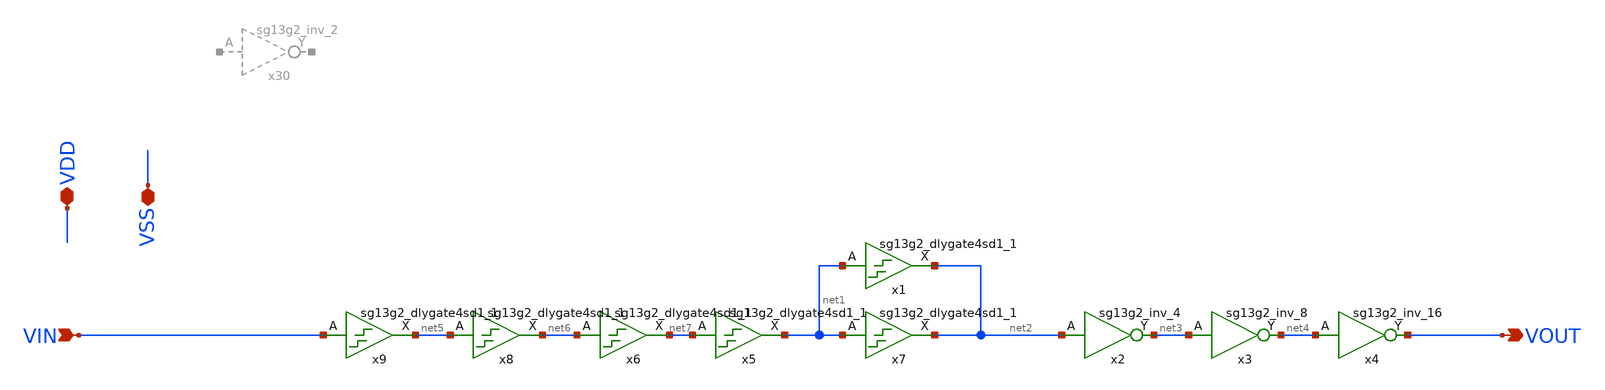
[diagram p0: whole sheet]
** sch_path: Cells/DLine.sch
* IHP-GmbH/IHP-Open-PDK/ihp-sg13g2/libs.tech/xschem/sg13g2_stdcells/sg13g2_inv_16.sch:
* Copyright 2023 IHP PDK Authors
* Licensed under the Apache License, Version 2.0 (the "License");
**.subckt DLine VOUT VIN VDD VSS
*.opin VOUT
*.ipin VIN
*.iopin VDD
*.iopin VSS
x7 net2 net1 VDD VSS sg13g2_dlygate4sd1_1
x1 net2 net1 VDD VSS sg13g2_dlygate4sd1_1
x2 net3 net2 VDD VSS sg13g2_inv_4
x3 net4 net3 VDD VSS sg13g2_inv_8
x4 VOUT net4 VDD VSS sg13g2_inv_16
x5 net1 net7 VDD VSS sg13g2_dlygate4sd1_1
x6 net7 net6 VDD VSS sg13g2_dlygate4sd1_1
x8 net6 net5 VDD VSS sg13g2_dlygate4sd1_1
x9 net5 VIN VDD VSS sg13g2_dlygate4sd1_1
**.ends

* expanding   symbol:  sg13g2_stdcells/sg13g2_dlygate4sd1_1.sym # of pins=2
** sym_path: sg13g2_stdcells/sg13g2_dlygate4sd1_1.sym
** sch_path: sg13g2_stdcells/sg13g2_dlygate4sd1_1.sch
.subckt sg13g2_dlygate4sd1_1 X A VDD VSS
*.ipin A
*.opin X
*.iopin VDD
*.iopin VSS
XM1 net2 A VSS VSS sg13_lv_nmos w=420.00n l=130.00n ng=1 m=1 mm_ok=1
XM2 net1 net2 VSS VSS sg13_lv_nmos w=420.00n l=130.00n ng=1 m=1 mm_ok=1
XM3 net3 net1 VSS VSS sg13_lv_nmos w=420.00n l=130.00n ng=1 m=1 mm_ok=1
XM4 X net3 VSS VSS sg13_lv_nmos w=740.00n l=130.00n ng=1 m=1 mm_ok=1
XM5 net2 A VDD VDD sg13_lv_pmos w=420.00n l=130.00n ng=1 m=1 mm_ok=1
XM6 net1 net2 VDD VDD sg13_lv_pmos w=1.000u l=130.00n ng=1 m=1 mm_ok=1
XM7 net3 net1 VDD VDD sg13_lv_pmos w=1.000u l=130.00n ng=1 m=1 mm_ok=1
XM8 X net3 VDD VDD sg13_lv_pmos w=1.12u l=130.00n ng=1 m=1 mm_ok=1
.ends


* expanding   symbol:  sg13g2_stdcells/sg13g2_inv_2.sym # of pins=2
** sym_path: sg13g2_stdcells/sg13g2_inv_2.sym
** sch_path: sg13g2_stdcells/sg13g2_inv_2.sch
.subckt sg13g2_inv_2 Y A VDD VSS
*.opin Y
*.ipin A
*.iopin VDD
*.iopin VSS
XM1 Y A VSS VSS sg13_lv_nmos w=1.48u l=130.00n ng=2 m=1 mm_ok=1
XM2 Y A VDD VDD sg13_lv_pmos w=2.24u l=130.00n ng=2 m=1 mm_ok=1
.ends


* expanding   symbol:  sg13g2_stdcells/sg13g2_inv_4.sym # of pins=2
** sym_path: sg13g2_stdcells/sg13g2_inv_4.sym
** sch_path: sg13g2_stdcells/sg13g2_inv_4.sch
.subckt sg13g2_inv_4 Y A VDD VSS
*.ipin A
*.opin Y
*.iopin VDD
*.iopin VSS
XM1 Y A VSS VSS sg13_lv_nmos w=2.96u l=130.00n ng=4 m=1 mm_ok=1
XM2 Y A VDD VDD sg13_lv_pmos w=4.48u l=130.00n ng=4 m=1 mm_ok=1
.ends


* expanding   symbol:  sg13g2_stdcells/sg13g2_inv_8.sym # of pins=2
** sym_path: sg13g2_stdcells/sg13g2_inv_8.sym
** sch_path: sg13g2_stdcells/sg13g2_inv_8.sch
.subckt sg13g2_inv_8 Y A VDD VSS
*.opin Y
*.ipin A
*.iopin VDD
*.iopin VSS
XM1 Y A VSS VSS sg13_lv_nmos w=5.92u l=130.00n ng=8 m=1 mm_ok=1
XM2 Y A VDD VDD sg13_lv_pmos w=8.96u l=130.00n ng=8 m=1 mm_ok=1
.ends


* expanding   symbol:  sg13g2_stdcells/sg13g2_inv_16.sym # of pins=2
** sym_path: sg13g2_stdcells/sg13g2_inv_16.sym
** sch_path: sg13g2_stdcells/sg13g2_inv_16.sch
.subckt sg13g2_inv_16 Y A VDD VSS
*.opin Y
*.iopin VSS
*.ipin A
*.iopin VDD
XM1 Y A VSS VSS sg13_lv_nmos w=11.84u l=130.00n ng=16 m=1 mm_ok=1
XM2 Y A VDD VDD sg13_lv_pmos w=17.92u l=130.00n ng=16 m=1 mm_ok=1
.ends

.end
